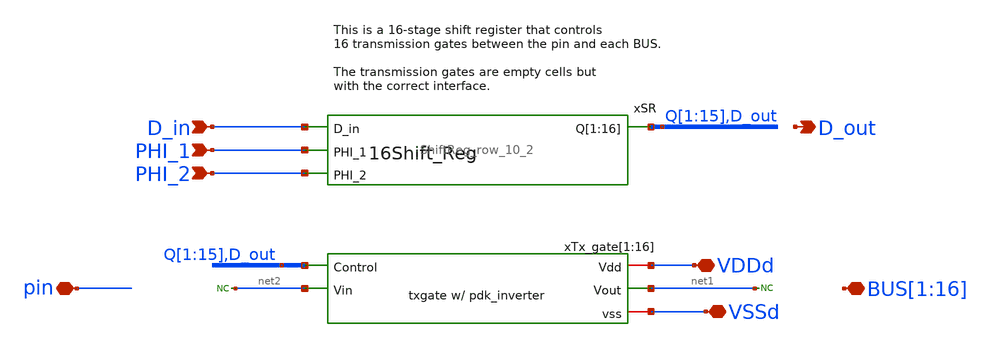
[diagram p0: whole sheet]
** sch_path: designs/libs/core_swmatrix/swmatrix_row_10.sch
**.subckt swmatrix_row_10 pin PHI_2 PHI_1
*+ BUS[1],BUS[2],BUS[3],BUS[4],BUS[5],BUS[6],BUS[7],BUS[8],BUS[9],BUS[10],BUS[11],BUS[12],BUS[13],BUS[14],BUS[15],BUS[16] D_in D_out VDDd VSSd
*.iopin pin
*.ipin PHI_2
*.ipin PHI_1
*.iopin
*+ BUS[1],BUS[2],BUS[3],BUS[4],BUS[5],BUS[6],BUS[7],BUS[8],BUS[9],BUS[10],BUS[11],BUS[12],BUS[13],BUS[14],BUS[15],BUS[16]
*.ipin D_in
*.opin D_out
*.iopin VDDd
*.iopin VSSd
xSR Q[1] Q[2] Q[3] Q[4] Q[5] Q[6] Q[7] Q[8] Q[9] Q[10] Q[11] Q[12] Q[13] Q[14] Q[15] D_out D_in
+ PHI_1 PHI_2 ShiftReg_row_10_2
xTx_gate[1] VDDd Q[1] net1 net2 VSSd transmission_gate_2
xTx_gate[2] VDDd Q[2] net1 net2 VSSd transmission_gate_2
xTx_gate[3] VDDd Q[3] net1 net2 VSSd transmission_gate_2
xTx_gate[4] VDDd Q[4] net1 net2 VSSd transmission_gate_2
xTx_gate[5] VDDd Q[5] net1 net2 VSSd transmission_gate_2
xTx_gate[6] VDDd Q[6] net1 net2 VSSd transmission_gate_2
xTx_gate[7] VDDd Q[7] net1 net2 VSSd transmission_gate_2
xTx_gate[8] VDDd Q[8] net1 net2 VSSd transmission_gate_2
xTx_gate[9] VDDd Q[9] net1 net2 VSSd transmission_gate_2
xTx_gate[10] VDDd Q[10] net1 net2 VSSd transmission_gate_2
xTx_gate[11] VDDd Q[11] net1 net2 VSSd transmission_gate_2
xTx_gate[12] VDDd Q[12] net1 net2 VSSd transmission_gate_2
xTx_gate[13] VDDd Q[13] net1 net2 VSSd transmission_gate_2
xTx_gate[14] VDDd Q[14] net1 net2 VSSd transmission_gate_2
xTx_gate[15] VDDd Q[15] net1 net2 VSSd transmission_gate_2
xTx_gate[16] VDDd D_out net1 net2 VSSd transmission_gate_2
* noconn #net2
* noconn #net1
**.ends
.end
